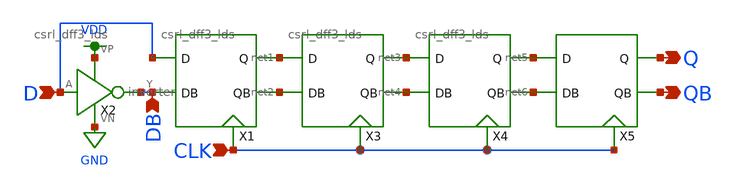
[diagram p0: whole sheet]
** sch_path: MP2/xschem/final/4reg.sch
**.subckt 4reg D CLK DB Q QB
*.ipin D
*.ipin CLK
*.ipin DB
*.opin Q
*.opin QB
X2 D DB VDD GND inverter
X1 D DB net1 net2 CLK csrl_dff3_lds
X3 net1 net2 net3 net4 CLK csrl_dff3_lds
X4 net3 net4 net5 net6 CLK csrl_dff3_lds
X5 net5 net6 Q QB CLK csrl_dff3_lds
**.ends
.GLOBAL GND
.GLOBAL VDD
.end
